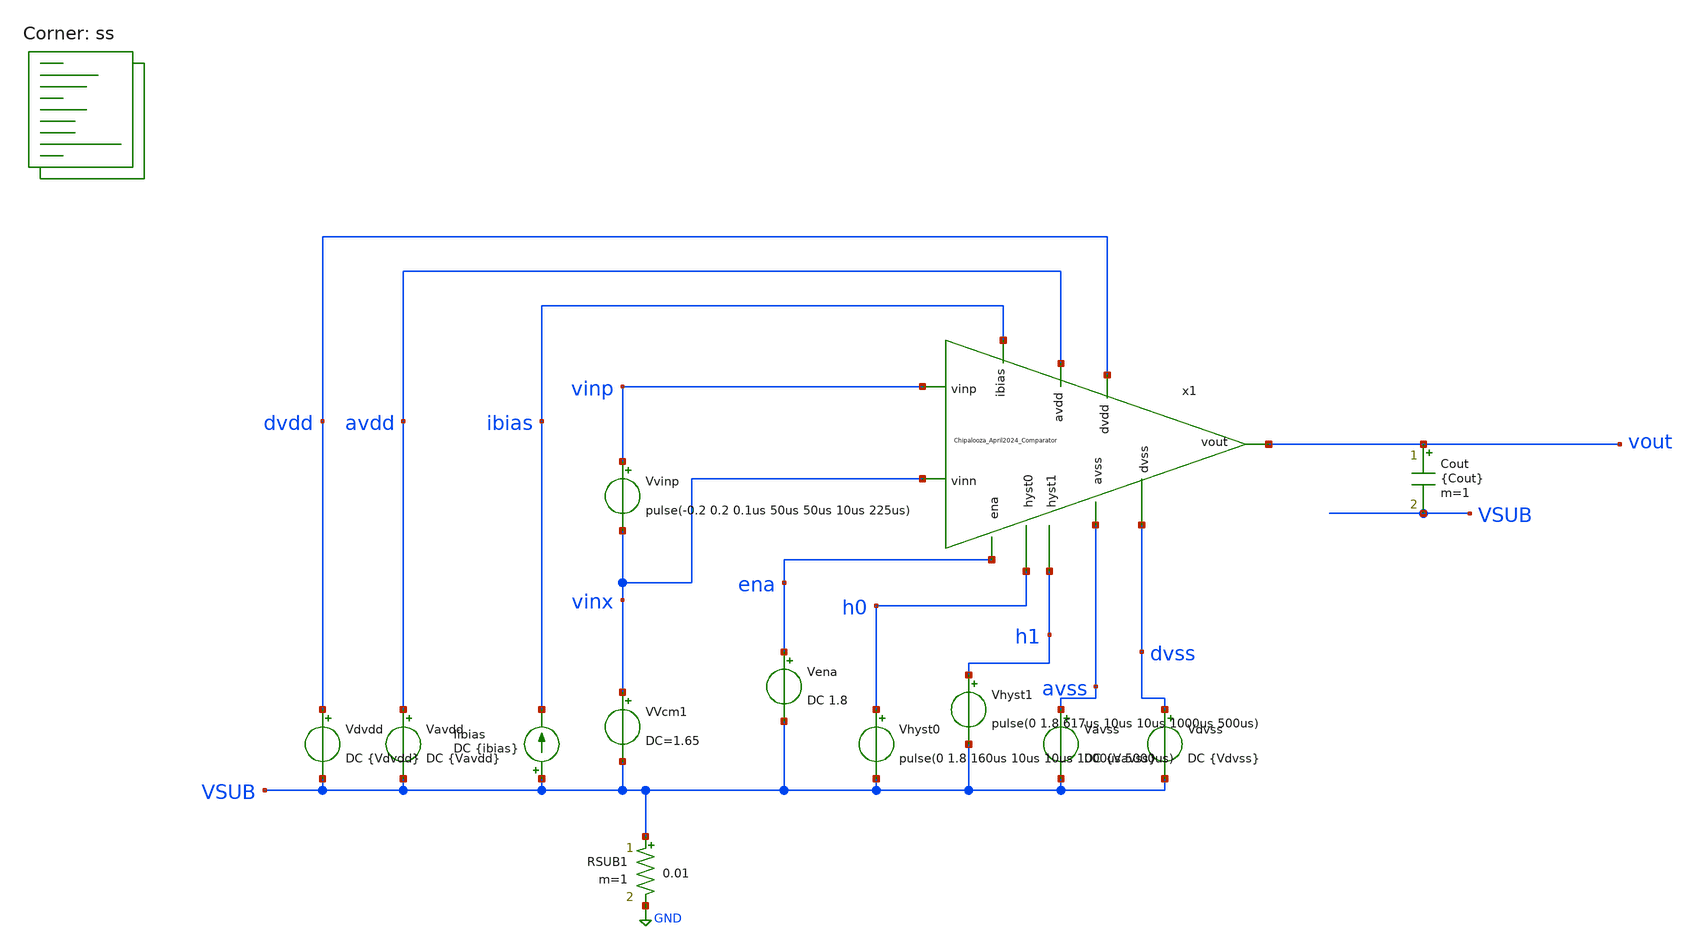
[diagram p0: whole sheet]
** sch_path: Chipalooza_April2024_Comparator/xschem/TB_hysteresis.sch
**.subckt TB_hysteresis
Vavdd avdd VSUB DC {Vavdd}
Vdvdd dvdd VSUB DC {Vdvdd}
Vena ena VSUB DC 1.8
Vhyst0 h0 VSUB pulse(0 1.8 160us 10us 10us 1000us 5000us)
Vhyst1 h1 VSUB pulse(0 1.8 617us 10us 10us 1000us 500us)
Vavss avss VSUB DC {Vavss}
Vdvss dvss VSUB DC {Vdvss}
Iibias VSUB ibias DC {ibias}
RSUB1 VSUB GND 0.01 m=1
VVcm1 vinx VSUB DC=1.65
Vvinp vinp vinx pulse(-0.2 0.2 0.1us 50us 50us 10us 225us)
x1 h0 h1 avdd vinp avss vinx dvdd dvss vout ibias ena Chipalooza_April2024_Comparator
Cout vout VSUB {Cout} m=1
**** begin user architecture code

* this option enables mos model bin
* selection based on W/NF instead of W
*.option wnflag=1
.option savecurrents
.option save all
.option temperature=25

.control

.param vavdd=3.3 cout=0 vdvdd=1.8 vavss=0
.param vdvss=0 ibias=1u

*dc VVcm 0 3.3 0.1
*plot v(vout) v(inx)

tran 0.1u 850u
*plot v(vout) v(vinp)

meas tran tr1 TRIG AT=0u TARG v(vout) VAL=1.75 RISE=1
meas tran vin_tr1 find v(vinp) at=tr1

meas tran tf1 TRIG AT=0u TARG v(vout) VAL=0.05 FALL=1
meas tran vin_tf1 find v(vinp) at=tf1

meas tran tr2 TRIG AT=0u TARG v(vout) VAL=1.75 RISE=2
meas tran vin_tr2 find v(vinp) at=tr1

meas tran tf2 TRIG AT=0u TARG v(vout) VAL=0.05 FALL=2
meas tran vin_tf2 find v(vinp) at=tf2

meas tran tr3 TRIG AT=0u TARG v(vout) VAL=1.75 RISE=3
meas tran vin_tr3 find v(vinp) at=tr3

meas tran tf3 TRIG AT=0u TARG v(vout) VAL=0.05 FALL=3
meas tran vin_tf3 find v(vinp) at=tf3

meas tran tr4 TRIG AT=0u TARG v(vout) VAL=1.75 RISE=4
meas tran vin_tr4 find v(vinp) at=tr4

meas tran tf4 TRIG AT=0u TARG v(vout) VAL=0.05 FALL=4
meas tran vin_tf4 find v(vinp) at=tf4

let hyst1=(vin_tf1-vin_tr1)
let hyst2=(vin_tf2-vin_tr2)
let hyst3=(vin_tf3-vin_tr3)
let hyst4=(vin_tf4-vin_tr4)

print hyst1
print hyst2
print hyst3
print hyst4

meas tran vinx_tr find v(vinx) at=tr1
let vio=(vinx_tr-vin_tr1)

print vio

write TB_hysteresis.raw

echo $&hyst1 $&hyst2 $&hyst3 $&vio > {simpath}/{filename}_{N}.data


*quit 0

.endc


.lib $::SKYWATER_MODELS/sky130.lib.spice ss
**** end user architecture code
**.ends

* expanding   symbol:  Chipalooza_April2024_Comparator.sym # of pins=11
** sym_path: Chipalooza_April2024_Comparator/xschem/Chipalooza_April2024_Comparator.sym
** sch_path: Chipalooza_April2024_Comparator/xschem/Chipalooza_April2024_Comparator.sch
.subckt Chipalooza_April2024_Comparator hyst0 hyst1 avdd vinp avss vinn dvdd dvss vout ibias ena
*.ipin vinp
*.ipin vinn
*.ipin hyst0
*.ipin hyst1
*.ipin avdd
*.ipin avss
*.ipin dvdd
*.ipin dvss
*.opin vout
*.ipin ena
*.ipin ibias
XM29 SumOutBar SumOut dvdd dvdd sky130_fd_pr__pfet_01v8 L=1 W=2 nf=1 ad='int((nf+1)/2) * W/nf * 0.29'
+ as='int((nf+2)/2) * W/nf * 0.29' pd='2*int((nf+1)/2) * (W/nf + 0.29)' ps='2*int((nf+2)/2) * (W/nf + 0.29)'
+ nrd='0.29 / W' nrs='0.29 / W' sa=0 sb=0 sd=0 mult=2 m=2
XM30 SumOutBar SumOut avssi dvss sky130_fd_pr__nfet_01v8 L=1 W=2 nf=1 ad='int((nf+1)/2) * W/nf * 0.29'
+ as='int((nf+2)/2) * W/nf * 0.29' pd='2*int((nf+1)/2) * (W/nf + 0.29)' ps='2*int((nf+2)/2) * (W/nf + 0.29)'
+ nrd='0.29 / W' nrs='0.29 / W' sa=0 sb=0 sd=0 mult=2 m=2
XM25 net3 ibias avssi avss sky130_fd_pr__nfet_g5v0d10v5 L=4 W=1 nf=1 ad='int((nf+1)/2) * W/nf * 0.29'
+ as='int((nf+2)/2) * W/nf * 0.29' pd='2*int((nf+1)/2) * (W/nf + 0.29)' ps='2*int((nf+2)/2) * (W/nf + 0.29)'
+ nrd='0.29 / W' nrs='0.29 / W' sa=0 sb=0 sd=0 mult=2 m=2
C1 avss 0 2p m=1
XM38 avssi ena avss avss sky130_fd_pr__nfet_g5v0d10v5 L=1 W=4 nf=1 ad='int((nf+1)/2) * W/nf * 0.29' as='int((nf+2)/2) * W/nf * 0.29'
+ pd='2*int((nf+1)/2) * (W/nf + 0.29)' ps='2*int((nf+2)/2) * (W/nf + 0.29)' nrd='0.29 / W' nrs='0.29 / W'
+ sa=0 sb=0 sd=0 mult=4 m=4
XM39 net4 ibias avssi avss sky130_fd_pr__nfet_g5v0d10v5 L=1 W=1 nf=1 ad='int((nf+1)/2) * W/nf * 0.29'
+ as='int((nf+2)/2) * W/nf * 0.29' pd='2*int((nf+1)/2) * (W/nf + 0.29)' ps='2*int((nf+2)/2) * (W/nf + 0.29)'
+ nrd='0.29 / W' nrs='0.29 / W' sa=0 sb=0 sd=0 mult=2 m=2
XM16 vout SumOutBar dvdd dvdd sky130_fd_pr__pfet_01v8 L=1 W=2 nf=1 ad='int((nf+1)/2) * W/nf * 0.29' as='int((nf+2)/2) * W/nf * 0.29'
+ pd='2*int((nf+1)/2) * (W/nf + 0.29)' ps='2*int((nf+2)/2) * (W/nf + 0.29)' nrd='0.29 / W' nrs='0.29 / W'
+ sa=0 sb=0 sd=0 mult=2 m=2
XM18 vout SumOutBar avssi dvss sky130_fd_pr__nfet_01v8 L=1 W=2 nf=1 ad='int((nf+1)/2) * W/nf * 0.29'
+ as='int((nf+2)/2) * W/nf * 0.29' pd='2*int((nf+1)/2) * (W/nf + 0.29)' ps='2*int((nf+2)/2) * (W/nf + 0.29)'
+ nrd='0.29 / W' nrs='0.29 / W' sa=0 sb=0 sd=0 mult=2 m=2
XM4 SourceBias2 SourceBias2 avdd avdd sky130_fd_pr__pfet_g5v0d10v5 L=1 W=2 nf=1 ad='int((nf+1)/2) * W/nf * 0.29'
+ as='int((nf+2)/2) * W/nf * 0.29' pd='2*int((nf+1)/2) * (W/nf + 0.29)' ps='2*int((nf+2)/2) * (W/nf + 0.29)'
+ nrd='0.29 / W' nrs='0.29 / W' sa=0 sb=0 sd=0 mult=2 m=2
XM5 N1 SourceBias2 avdd avdd sky130_fd_pr__pfet_g5v0d10v5 L=1 W=2 nf=1 ad='int((nf+1)/2) * W/nf * 0.29'
+ as='int((nf+2)/2) * W/nf * 0.29' pd='2*int((nf+1)/2) * (W/nf + 0.29)' ps='2*int((nf+2)/2) * (W/nf + 0.29)'
+ nrd='0.29 / W' nrs='0.29 / W' sa=0 sb=0 sd=0 mult=2 m=2
XM6 N2 SourceBias2 avdd avdd sky130_fd_pr__pfet_g5v0d10v5 L=1 W=2 nf=1 ad='int((nf+1)/2) * W/nf * 0.29'
+ as='int((nf+2)/2) * W/nf * 0.29' pd='2*int((nf+1)/2) * (W/nf + 0.29)' ps='2*int((nf+2)/2) * (W/nf + 0.29)'
+ nrd='0.29 / W' nrs='0.29 / W' sa=0 sb=0 sd=0 mult=2 m=2
XM7 SumOut Bias1 N2 avdd sky130_fd_pr__pfet_g5v0d10v5 L=1 W=2 nf=1 ad='int((nf+1)/2) * W/nf * 0.29' as='int((nf+2)/2) * W/nf * 0.29'
+ pd='2*int((nf+1)/2) * (W/nf + 0.29)' ps='2*int((nf+2)/2) * (W/nf + 0.29)' nrd='0.29 / W' nrs='0.29 / W'
+ sa=0 sb=0 sd=0 mult=2 m=2
XM8 Sum Bias1 N1 avdd sky130_fd_pr__pfet_g5v0d10v5 L=1 W=2 nf=1 ad='int((nf+1)/2) * W/nf * 0.29' as='int((nf+2)/2) * W/nf * 0.29'
+ pd='2*int((nf+1)/2) * (W/nf + 0.29)' ps='2*int((nf+2)/2) * (W/nf + 0.29)' nrd='0.29 / W' nrs='0.29 / W'
+ sa=0 sb=0 sd=0 mult=2 m=2
XM9 SumOut Bias2 P2 avss sky130_fd_pr__nfet_g5v0d10v5 L=1 W=2 nf=1 ad='int((nf+1)/2) * W/nf * 0.29' as='int((nf+2)/2) * W/nf * 0.29'
+ pd='2*int((nf+1)/2) * (W/nf + 0.29)' ps='2*int((nf+2)/2) * (W/nf + 0.29)' nrd='0.29 / W' nrs='0.29 / W'
+ sa=0 sb=0 sd=0 mult=2 m=2
XM10 Sum Bias2 P1 avss sky130_fd_pr__nfet_g5v0d10v5 L=1 W=2 nf=1 ad='int((nf+1)/2) * W/nf * 0.29' as='int((nf+2)/2) * W/nf * 0.29'
+ pd='2*int((nf+1)/2) * (W/nf + 0.29)' ps='2*int((nf+2)/2) * (W/nf + 0.29)' nrd='0.29 / W' nrs='0.29 / W'
+ sa=0 sb=0 sd=0 mult=2 m=2
XM11 P2 Sum avssi avss sky130_fd_pr__nfet_g5v0d10v5 L=1 W=2 nf=1 ad='int((nf+1)/2) * W/nf * 0.29' as='int((nf+2)/2) * W/nf * 0.29'
+ pd='2*int((nf+1)/2) * (W/nf + 0.29)' ps='2*int((nf+2)/2) * (W/nf + 0.29)' nrd='0.29 / W' nrs='0.29 / W'
+ sa=0 sb=0 sd=0 mult=2 m=2
XM12 P1 Sum avssi avss sky130_fd_pr__nfet_g5v0d10v5 L=1 W=2 nf=1 ad='int((nf+1)/2) * W/nf * 0.29' as='int((nf+2)/2) * W/nf * 0.29'
+ pd='2*int((nf+1)/2) * (W/nf + 0.29)' ps='2*int((nf+2)/2) * (W/nf + 0.29)' nrd='0.29 / W' nrs='0.29 / W'
+ sa=0 sb=0 sd=0 mult=2 m=2
XM2 P2 vinn psource_input avdd sky130_fd_pr__pfet_g5v0d10v5 L=1 W=4 nf=1 ad='int((nf+1)/2) * W/nf * 0.29'
+ as='int((nf+2)/2) * W/nf * 0.29' pd='2*int((nf+1)/2) * (W/nf + 0.29)' ps='2*int((nf+2)/2) * (W/nf + 0.29)'
+ nrd='0.29 / W' nrs='0.29 / W' sa=0 sb=0 sd=0 mult=2 m=2
XM3 P1 vinp psource_input avdd sky130_fd_pr__pfet_g5v0d10v5 L=1 W=4 nf=1 ad='int((nf+1)/2) * W/nf * 0.29'
+ as='int((nf+2)/2) * W/nf * 0.29' pd='2*int((nf+1)/2) * (W/nf + 0.29)' ps='2*int((nf+2)/2) * (W/nf + 0.29)'
+ nrd='0.29 / W' nrs='0.29 / W' sa=0 sb=0 sd=0 mult=2 m=2
XM14 psource_input net5 avdd avdd sky130_fd_pr__pfet_g5v0d10v5 L=1 W=12 nf=1 ad='int((nf+1)/2) * W/nf * 0.29'
+ as='int((nf+2)/2) * W/nf * 0.29' pd='2*int((nf+1)/2) * (W/nf + 0.29)' ps='2*int((nf+2)/2) * (W/nf + 0.29)'
+ nrd='0.29 / W' nrs='0.29 / W' sa=0 sb=0 sd=0 mult=4 m=4
XM15 net5 net5 avdd avdd sky130_fd_pr__pfet_g5v0d10v5 L=1 W=8 nf=1 ad='int((nf+1)/2) * W/nf * 0.29' as='int((nf+2)/2) * W/nf * 0.29'
+ pd='2*int((nf+1)/2) * (W/nf + 0.29)' ps='2*int((nf+2)/2) * (W/nf + 0.29)' nrd='0.29 / W' nrs='0.29 / W'
+ sa=0 sb=0 sd=0 mult=2 m=2
XM17 nbias_tail net10 psource_input avdd sky130_fd_pr__pfet_g5v0d10v5 L=1 W=8 nf=1 ad='int((nf+1)/2) * W/nf * 0.29'
+ as='int((nf+2)/2) * W/nf * 0.29' pd='2*int((nf+1)/2) * (W/nf + 0.29)' ps='2*int((nf+2)/2) * (W/nf + 0.29)'
+ nrd='0.29 / W' nrs='0.29 / W' sa=0 sb=0 sd=0 mult=2 m=2
XM20 N1 vinp SourceBias0 avss sky130_fd_pr__nfet_g5v0d10v5 L=4 W=16 nf=1 ad='int((nf+1)/2) * W/nf * 0.29'
+ as='int((nf+2)/2) * W/nf * 0.29' pd='2*int((nf+1)/2) * (W/nf + 0.29)' ps='2*int((nf+2)/2) * (W/nf + 0.29)'
+ nrd='0.29 / W' nrs='0.29 / W' sa=0 sb=0 sd=0 mult=2 m=2
XM21 N2 vinn SourceBias0 avss sky130_fd_pr__nfet_g5v0d10v5 L=4 W=16 nf=1 ad='int((nf+1)/2) * W/nf * 0.29'
+ as='int((nf+2)/2) * W/nf * 0.29' pd='2*int((nf+1)/2) * (W/nf + 0.29)' ps='2*int((nf+2)/2) * (W/nf + 0.29)'
+ nrd='0.29 / W' nrs='0.29 / W' sa=0 sb=0 sd=0 mult=2 m=2
XM22 SourceBias0 nbias_tail avssi avss sky130_fd_pr__nfet_g5v0d10v5 L=1 W=12 nf=1 ad='int((nf+1)/2) * W/nf * 0.29'
+ as='int((nf+2)/2) * W/nf * 0.29' pd='2*int((nf+1)/2) * (W/nf + 0.29)' ps='2*int((nf+2)/2) * (W/nf + 0.29)'
+ nrd='0.29 / W' nrs='0.29 / W' sa=0 sb=0 sd=0 mult=4 m=4
XM23 nbias_tail nbias_tail avssi avss sky130_fd_pr__nfet_g5v0d10v5 L=1 W=12 nf=1 ad='int((nf+1)/2) * W/nf * 0.29'
+ as='int((nf+2)/2) * W/nf * 0.29' pd='2*int((nf+1)/2) * (W/nf + 0.29)' ps='2*int((nf+2)/2) * (W/nf + 0.29)'
+ nrd='0.29 / W' nrs='0.29 / W' sa=0 sb=0 sd=0 mult=2 m=2
XM28 net5 Bias5 SourceBias0 avss sky130_fd_pr__nfet_g5v0d10v5 L=1 W=4 nf=1 ad='int((nf+1)/2) * W/nf * 0.29'
+ as='int((nf+2)/2) * W/nf * 0.29' pd='2*int((nf+1)/2) * (W/nf + 0.29)' ps='2*int((nf+2)/2) * (W/nf + 0.29)'
+ nrd='0.29 / W' nrs='0.29 / W' sa=0 sb=0 sd=0 mult=2 m=2
XM45 SourceBias1 ibias avssi avss sky130_fd_pr__nfet_g5v0d10v5 L=1 W=3 nf=1 ad='int((nf+1)/2) * W/nf * 0.29'
+ as='int((nf+2)/2) * W/nf * 0.29' pd='2*int((nf+1)/2) * (W/nf + 0.29)' ps='2*int((nf+2)/2) * (W/nf + 0.29)'
+ nrd='0.29 / W' nrs='0.29 / W' sa=0 sb=0 sd=0 mult=2 m=2
XM46 SourceBias1 SourceBias1 avdd avdd sky130_fd_pr__pfet_g5v0d10v5 L=1 W=12 nf=1 ad='int((nf+1)/2) * W/nf * 0.29'
+ as='int((nf+2)/2) * W/nf * 0.29' pd='2*int((nf+1)/2) * (W/nf + 0.29)' ps='2*int((nf+2)/2) * (W/nf + 0.29)'
+ nrd='0.29 / W' nrs='0.29 / W' sa=0 sb=0 sd=0 mult=4 m=4
XM47 psource_input SourceBias1 avdd avdd sky130_fd_pr__pfet_g5v0d10v5 L=1 W=12 nf=1 ad='int((nf+1)/2) * W/nf * 0.29'
+ as='int((nf+2)/2) * W/nf * 0.29' pd='2*int((nf+1)/2) * (W/nf + 0.29)' ps='2*int((nf+2)/2) * (W/nf + 0.29)'
+ nrd='0.29 / W' nrs='0.29 / W' sa=0 sb=0 sd=0 mult=4 m=4
XM48 SourceBias2 ibias avssi avss sky130_fd_pr__nfet_g5v0d10v5 L=1 W=6 nf=1 ad='int((nf+1)/2) * W/nf * 0.29'
+ as='int((nf+2)/2) * W/nf * 0.29' pd='2*int((nf+1)/2) * (W/nf + 0.29)' ps='2*int((nf+2)/2) * (W/nf + 0.29)'
+ nrd='0.29 / W' nrs='0.29 / W' sa=0 sb=0 sd=0 mult=2 m=2
XM65 SourceBias3 ibias avssi avss sky130_fd_pr__nfet_g5v0d10v5 L=1 W=1 nf=1 ad='int((nf+1)/2) * W/nf * 0.29'
+ as='int((nf+2)/2) * W/nf * 0.29' pd='2*int((nf+1)/2) * (W/nf + 0.29)' ps='2*int((nf+2)/2) * (W/nf + 0.29)'
+ nrd='0.29 / W' nrs='0.29 / W' sa=0 sb=0 sd=0 mult=2 m=2
XM76 Bias1 ibias avssi avss sky130_fd_pr__nfet_g5v0d10v5 L=1 W=3 nf=1 ad='int((nf+1)/2) * W/nf * 0.29'
+ as='int((nf+2)/2) * W/nf * 0.29' pd='2*int((nf+1)/2) * (W/nf + 0.29)' ps='2*int((nf+2)/2) * (W/nf + 0.29)'
+ nrd='0.29 / W' nrs='0.29 / W' sa=0 sb=0 sd=0 mult=2 m=2
XM77 SourceBias5 ibias avssi avss sky130_fd_pr__nfet_g5v0d10v5 L=1 W=3 nf=1 ad='int((nf+1)/2) * W/nf * 0.29'
+ as='int((nf+2)/2) * W/nf * 0.29' pd='2*int((nf+1)/2) * (W/nf + 0.29)' ps='2*int((nf+2)/2) * (W/nf + 0.29)'
+ nrd='0.29 / W' nrs='0.29 / W' sa=0 sb=0 sd=0 mult=2 m=2
XM78 SourceBias6 ibias avssi avss sky130_fd_pr__nfet_g5v0d10v5 L=1 W=3 nf=1 ad='int((nf+1)/2) * W/nf * 0.29'
+ as='int((nf+2)/2) * W/nf * 0.29' pd='2*int((nf+1)/2) * (W/nf + 0.29)' ps='2*int((nf+2)/2) * (W/nf + 0.29)'
+ nrd='0.29 / W' nrs='0.29 / W' sa=0 sb=0 sd=0 mult=2 m=2
XM79 SourceBias7 ibias avssi avss sky130_fd_pr__nfet_g5v0d10v5 L=1 W=3 nf=1 ad='int((nf+1)/2) * W/nf * 0.29'
+ as='int((nf+2)/2) * W/nf * 0.29' pd='2*int((nf+1)/2) * (W/nf + 0.29)' ps='2*int((nf+2)/2) * (W/nf + 0.29)'
+ nrd='0.29 / W' nrs='0.29 / W' sa=0 sb=0 sd=0 mult=2 m=2
XM81 Bias5 ibias avssi avss sky130_fd_pr__nfet_g5v0d10v5 L=1 W=3 nf=1 ad='int((nf+1)/2) * W/nf * 0.29'
+ as='int((nf+2)/2) * W/nf * 0.29' pd='2*int((nf+1)/2) * (W/nf + 0.29)' ps='2*int((nf+2)/2) * (W/nf + 0.29)'
+ nrd='0.29 / W' nrs='0.29 / W' sa=0 sb=0 sd=0 mult=2 m=2
XM54 M55Source M55Drain avssi avss sky130_fd_pr__nfet_g5v0d10v5 L=1.5 W=6 nf=1 ad='int((nf+1)/2) * W/nf * 0.29'
+ as='int((nf+2)/2) * W/nf * 0.29' pd='2*int((nf+1)/2) * (W/nf + 0.29)' ps='2*int((nf+2)/2) * (W/nf + 0.29)'
+ nrd='0.29 / W' nrs='0.29 / W' sa=0 sb=0 sd=0 mult=2 m=2
XM55 M55Drain Bias2 M55Source avss sky130_fd_pr__nfet_g5v0d10v5 L=1 W=9 nf=1 ad='int((nf+1)/2) * W/nf * 0.29'
+ as='int((nf+2)/2) * W/nf * 0.29' pd='2*int((nf+1)/2) * (W/nf + 0.29)' ps='2*int((nf+2)/2) * (W/nf + 0.29)'
+ nrd='0.29 / W' nrs='0.29 / W' sa=0 sb=0 sd=0 mult=2 m=2
XM56 Bias2 Bias2 avssi avss sky130_fd_pr__nfet_g5v0d10v5 L=2 W=0.5 nf=1 ad='int((nf+1)/2) * W/nf * 0.29'
+ as='int((nf+2)/2) * W/nf * 0.29' pd='2*int((nf+1)/2) * (W/nf + 0.29)' ps='2*int((nf+2)/2) * (W/nf + 0.29)'
+ nrd='0.29 / W' nrs='0.29 / W' sa=0 sb=0 sd=0 mult=1 m=1
XM51 net6 net7 avdd avdd sky130_fd_pr__pfet_g5v0d10v5 L=2 W=20 nf=1 ad='int((nf+1)/2) * W/nf * 0.29'
+ as='int((nf+2)/2) * W/nf * 0.29' pd='2*int((nf+1)/2) * (W/nf + 0.29)' ps='2*int((nf+2)/2) * (W/nf + 0.29)'
+ nrd='0.29 / W' nrs='0.29 / W' sa=0 sb=0 sd=0 mult=2 m=2
XM49 net7 net7 avdd avdd sky130_fd_pr__pfet_g5v0d10v5 L=2 W=10 nf=1 ad='int((nf+1)/2) * W/nf * 0.29'
+ as='int((nf+2)/2) * W/nf * 0.29' pd='2*int((nf+1)/2) * (W/nf + 0.29)' ps='2*int((nf+2)/2) * (W/nf + 0.29)'
+ nrd='0.29 / W' nrs='0.29 / W' sa=0 sb=0 sd=0 mult=2 m=2
XM50 SourceBias4 SourceBias4 net7 avdd sky130_fd_pr__pfet_g5v0d10v5 L=1 W=10 nf=1 ad='int((nf+1)/2) * W/nf * 0.29'
+ as='int((nf+2)/2) * W/nf * 0.29' pd='2*int((nf+1)/2) * (W/nf + 0.29)' ps='2*int((nf+2)/2) * (W/nf + 0.29)'
+ nrd='0.29 / W' nrs='0.29 / W' sa=0 sb=0 sd=0 mult=2 m=2
XM52 avssi SourceBias4 net6 avdd sky130_fd_pr__pfet_g5v0d10v5 L=1 W=1 nf=1 ad='int((nf+1)/2) * W/nf * 0.29'
+ as='int((nf+2)/2) * W/nf * 0.29' pd='2*int((nf+1)/2) * (W/nf + 0.29)' ps='2*int((nf+2)/2) * (W/nf + 0.29)'
+ nrd='0.29 / W' nrs='0.29 / W' sa=0 sb=0 sd=0 mult=2 m=2
XM53 Bias1 Bias1 net6 avdd sky130_fd_pr__pfet_g5v0d10v5 L=1 W=5 nf=1 ad='int((nf+1)/2) * W/nf * 0.29'
+ as='int((nf+2)/2) * W/nf * 0.29' pd='2*int((nf+1)/2) * (W/nf + 0.29)' ps='2*int((nf+2)/2) * (W/nf + 0.29)'
+ nrd='0.29 / W' nrs='0.29 / W' sa=0 sb=0 sd=0 mult=2 m=2
XM66 net8 net9 avdd avdd sky130_fd_pr__pfet_g5v0d10v5 L=2 W=20 nf=1 ad='int((nf+1)/2) * W/nf * 0.29'
+ as='int((nf+2)/2) * W/nf * 0.29' pd='2*int((nf+1)/2) * (W/nf + 0.29)' ps='2*int((nf+2)/2) * (W/nf + 0.29)'
+ nrd='0.29 / W' nrs='0.29 / W' sa=0 sb=0 sd=0 mult=2 m=2
XM67 net9 net9 avdd avdd sky130_fd_pr__pfet_g5v0d10v5 L=2 W=20 nf=1 ad='int((nf+1)/2) * W/nf * 0.29'
+ as='int((nf+2)/2) * W/nf * 0.29' pd='2*int((nf+1)/2) * (W/nf + 0.29)' ps='2*int((nf+2)/2) * (W/nf + 0.29)'
+ nrd='0.29 / W' nrs='0.29 / W' sa=0 sb=0 sd=0 mult=2 m=2
XM68 SourceBias7 SourceBias7 net9 avdd sky130_fd_pr__pfet_g5v0d10v5 L=1 W=10 nf=1 ad='int((nf+1)/2) * W/nf * 0.29'
+ as='int((nf+2)/2) * W/nf * 0.29' pd='2*int((nf+1)/2) * (W/nf + 0.29)' ps='2*int((nf+2)/2) * (W/nf + 0.29)'
+ nrd='0.29 / W' nrs='0.29 / W' sa=0 sb=0 sd=0 mult=2 m=2
XM69 avssi SourceBias7 net8 avdd sky130_fd_pr__pfet_g5v0d10v5 L=1 W=1 nf=1 ad='int((nf+1)/2) * W/nf * 0.29'
+ as='int((nf+2)/2) * W/nf * 0.29' pd='2*int((nf+1)/2) * (W/nf + 0.29)' ps='2*int((nf+2)/2) * (W/nf + 0.29)'
+ nrd='0.29 / W' nrs='0.29 / W' sa=0 sb=0 sd=0 mult=2 m=2
XM70 Bias5 Bias5 net8 avdd sky130_fd_pr__pfet_g5v0d10v5 L=1 W=5 nf=1 ad='int((nf+1)/2) * W/nf * 0.29'
+ as='int((nf+2)/2) * W/nf * 0.29' pd='2*int((nf+1)/2) * (W/nf + 0.29)' ps='2*int((nf+2)/2) * (W/nf + 0.29)'
+ nrd='0.29 / W' nrs='0.29 / W' sa=0 sb=0 sd=0 mult=2 m=2
XM72 SourceBias5 SourceBias5 avdd avdd sky130_fd_pr__pfet_g5v0d10v5 L=1 W=12 nf=1 ad='int((nf+1)/2) * W/nf * 0.29'
+ as='int((nf+2)/2) * W/nf * 0.29' pd='2*int((nf+1)/2) * (W/nf + 0.29)' ps='2*int((nf+2)/2) * (W/nf + 0.29)'
+ nrd='0.29 / W' nrs='0.29 / W' sa=0 sb=0 sd=0 mult=4 m=4
XM73 M55Drain SourceBias5 avdd avdd sky130_fd_pr__pfet_g5v0d10v5 L=1 W=12 nf=1 ad='int((nf+1)/2) * W/nf * 0.29'
+ as='int((nf+2)/2) * W/nf * 0.29' pd='2*int((nf+1)/2) * (W/nf + 0.29)' ps='2*int((nf+2)/2) * (W/nf + 0.29)'
+ nrd='0.29 / W' nrs='0.29 / W' sa=0 sb=0 sd=0 mult=4 m=4
XM74 SourceBias6 SourceBias6 avdd avdd sky130_fd_pr__pfet_g5v0d10v5 L=1 W=12 nf=1 ad='int((nf+1)/2) * W/nf * 0.29'
+ as='int((nf+2)/2) * W/nf * 0.29' pd='2*int((nf+1)/2) * (W/nf + 0.29)' ps='2*int((nf+2)/2) * (W/nf + 0.29)'
+ nrd='0.29 / W' nrs='0.29 / W' sa=0 sb=0 sd=0 mult=4 m=4
XM75 Bias2 SourceBias6 avdd avdd sky130_fd_pr__pfet_g5v0d10v5 L=1 W=12 nf=1 ad='int((nf+1)/2) * W/nf * 0.29'
+ as='int((nf+2)/2) * W/nf * 0.29' pd='2*int((nf+1)/2) * (W/nf + 0.29)' ps='2*int((nf+2)/2) * (W/nf + 0.29)'
+ nrd='0.29 / W' nrs='0.29 / W' sa=0 sb=0 sd=0 mult=4 m=4
XM1 SourceBias0 ibias avssi avss sky130_fd_pr__nfet_g5v0d10v5 L=1 W=3 nf=1 ad='int((nf+1)/2) * W/nf * 0.29'
+ as='int((nf+2)/2) * W/nf * 0.29' pd='2*int((nf+1)/2) * (W/nf + 0.29)' ps='2*int((nf+2)/2) * (W/nf + 0.29)'
+ nrd='0.29 / W' nrs='0.29 / W' sa=0 sb=0 sd=0 mult=2 m=2
XM31 net1 hyst0 net3 avss sky130_fd_pr__nfet_01v8 L=4 W=1 nf=1 ad='int((1 + 1)/2) * 1 / 1 * 0.29' as='int((1 + 2)/2) * 1 / 1 * 0.29'
+ pd='2*int((1 + 1)/2) * (1 / 1 + 0.29)' ps='2*int((1 + 2)/2) * (1 / 1 + 0.29)' nrd='0.29 / 1 ' nrs='0.29 / 1 '
+ sa=0 sb=0 sd=0 mult=2 m=2
XM32 net1 hyst1 net4 avss sky130_fd_pr__nfet_01v8 L=1 W=1 nf=1 ad='int((1 + 1)/2) * 1 / 1 * 0.29' as='int((1 + 2)/2) * 1 / 1 * 0.29'
+ pd='2*int((1 + 1)/2) * (1 / 1 + 0.29)' ps='2*int((1 + 2)/2) * (1 / 1 + 0.29)' nrd='0.29 / 1 ' nrs='0.29 / 1 '
+ sa=0 sb=0 sd=0 mult=2 m=2
XM19 N1 SumOut net1 avss sky130_fd_pr__nfet_g5v0d10v5 L=1 W=2 nf=1 ad='int((nf+1)/2) * W/nf * 0.29' as='int((nf+2)/2) * W/nf * 0.29'
+ pd='2*int((nf+1)/2) * (W/nf + 0.29)' ps='2*int((nf+2)/2) * (W/nf + 0.29)' nrd='0.29 / W' nrs='0.29 / W'
+ sa=0 sb=0 sd=0 mult=2 m=2
XM24 N2 SumOutBar net1 avss sky130_fd_pr__nfet_g5v0d10v5 L=1 W=2 nf=1 ad='int((nf+1)/2) * W/nf * 0.29'
+ as='int((nf+2)/2) * W/nf * 0.29' pd='2*int((nf+1)/2) * (W/nf + 0.29)' ps='2*int((nf+2)/2) * (W/nf + 0.29)'
+ nrd='0.29 / W' nrs='0.29 / W' sa=0 sb=0 sd=0 mult=2 m=2
XM26 ibias ibias avssi avss sky130_fd_pr__nfet_g5v0d10v5 L=1 W=3 nf=1 ad='int((nf+1)/2) * W/nf * 0.29'
+ as='int((nf+2)/2) * W/nf * 0.29' pd='2*int((nf+1)/2) * (W/nf + 0.29)' ps='2*int((nf+2)/2) * (W/nf + 0.29)'
+ nrd='0.29 / W' nrs='0.29 / W' sa=0 sb=0 sd=0 mult=2 m=2
XM27 net2 ibias avssi avss sky130_fd_pr__nfet_g5v0d10v5 L=1 W=3 nf=1 ad='int((nf+1)/2) * W/nf * 0.29'
+ as='int((nf+2)/2) * W/nf * 0.29' pd='2*int((nf+1)/2) * (W/nf + 0.29)' ps='2*int((nf+2)/2) * (W/nf + 0.29)'
+ nrd='0.29 / W' nrs='0.29 / W' sa=0 sb=0 sd=0 mult=2 m=2
XM33 net2 net2 avdd avdd sky130_fd_pr__pfet_g5v0d10v5 L=1 W=3 nf=1 ad='int((nf+1)/2) * W/nf * 0.29' as='int((nf+2)/2) * W/nf * 0.29'
+ pd='2*int((nf+1)/2) * (W/nf + 0.29)' ps='2*int((nf+2)/2) * (W/nf + 0.29)' nrd='0.29 / W' nrs='0.29 / W'
+ sa=0 sb=0 sd=0 mult=2 m=2
XM34 avss net2 avdd avdd sky130_fd_pr__pfet_g5v0d10v5 L=1 W=3 nf=1 ad='int((nf+1)/2) * W/nf * 0.29' as='int((nf+2)/2) * W/nf * 0.29'
+ pd='2*int((nf+1)/2) * (W/nf + 0.29)' ps='2*int((nf+2)/2) * (W/nf + 0.29)' nrd='0.29 / W' nrs='0.29 / W'
+ sa=0 sb=0 sd=0 mult=2 m=2
XM63 net10 net10 avdd avdd sky130_fd_pr__pfet_g5v0d10v5 L=5 W=3 nf=1 ad='int((nf+1)/2) * W/nf * 0.29'
+ as='int((nf+2)/2) * W/nf * 0.29' pd='2*int((nf+1)/2) * (W/nf + 0.29)' ps='2*int((nf+2)/2) * (W/nf + 0.29)'
+ nrd='0.29 / W' nrs='0.29 / W' sa=0 sb=0 sd=0 mult=1 m=1
XM62 avdd Bias4 SourceBias3 avss sky130_fd_pr__nfet_g5v0d10v5 L=1 W=4 nf=1 ad='int((nf+1)/2) * W/nf * 0.29'
+ as='int((nf+2)/2) * W/nf * 0.29' pd='2*int((nf+1)/2) * (W/nf + 0.29)' ps='2*int((nf+2)/2) * (W/nf + 0.29)'
+ nrd='0.29 / W' nrs='0.29 / W' sa=0 sb=0 sd=0 mult=2 m=2
XM64 net10 Bias5 SourceBias3 avss sky130_fd_pr__nfet_g5v0d10v5 L=1 W=4 nf=1 ad='int((nf+1)/2) * W/nf * 0.29'
+ as='int((nf+2)/2) * W/nf * 0.29' pd='2*int((nf+1)/2) * (W/nf + 0.29)' ps='2*int((nf+2)/2) * (W/nf + 0.29)'
+ nrd='0.29 / W' nrs='0.29 / W' sa=0 sb=0 sd=0 mult=2 m=2
XM57 net11 net12 avdd avdd sky130_fd_pr__pfet_g5v0d10v5 L=2 W=20 nf=1 ad='int((nf+1)/2) * W/nf * 0.29'
+ as='int((nf+2)/2) * W/nf * 0.29' pd='2*int((nf+1)/2) * (W/nf + 0.29)' ps='2*int((nf+2)/2) * (W/nf + 0.29)'
+ nrd='0.29 / W' nrs='0.29 / W' sa=0 sb=0 sd=0 mult=2 m=2
XM58 net12 net12 avdd avdd sky130_fd_pr__pfet_g5v0d10v5 L=2 W=10 nf=1 ad='int((nf+1)/2) * W/nf * 0.29'
+ as='int((nf+2)/2) * W/nf * 0.29' pd='2*int((nf+1)/2) * (W/nf + 0.29)' ps='2*int((nf+2)/2) * (W/nf + 0.29)'
+ nrd='0.29 / W' nrs='0.29 / W' sa=0 sb=0 sd=0 mult=2 m=2
XM59 SourceBias10 SourceBias10 net12 avdd sky130_fd_pr__pfet_g5v0d10v5 L=1 W=10 nf=1 ad='int((nf+1)/2) * W/nf * 0.29'
+ as='int((nf+2)/2) * W/nf * 0.29' pd='2*int((nf+1)/2) * (W/nf + 0.29)' ps='2*int((nf+2)/2) * (W/nf + 0.29)'
+ nrd='0.29 / W' nrs='0.29 / W' sa=0 sb=0 sd=0 mult=2 m=2
XM60 avss SourceBias10 net11 avdd sky130_fd_pr__pfet_g5v0d10v5 L=1 W=1 nf=1 ad='int((nf+1)/2) * W/nf * 0.29'
+ as='int((nf+2)/2) * W/nf * 0.29' pd='2*int((nf+1)/2) * (W/nf + 0.29)' ps='2*int((nf+2)/2) * (W/nf + 0.29)'
+ nrd='0.29 / W' nrs='0.29 / W' sa=0 sb=0 sd=0 mult=2 m=2
XM61 Bias4 Bias4 net11 avdd sky130_fd_pr__pfet_g5v0d10v5 L=1 W=5 nf=1 ad='int((nf+1)/2) * W/nf * 0.29'
+ as='int((nf+2)/2) * W/nf * 0.29' pd='2*int((nf+1)/2) * (W/nf + 0.29)' ps='2*int((nf+2)/2) * (W/nf + 0.29)'
+ nrd='0.29 / W' nrs='0.29 / W' sa=0 sb=0 sd=0 mult=2 m=2
XM13 Bias4 ibias avssi avss sky130_fd_pr__nfet_g5v0d10v5 L=1 W=3 nf=1 ad='int((nf+1)/2) * W/nf * 0.29'
+ as='int((nf+2)/2) * W/nf * 0.29' pd='2*int((nf+1)/2) * (W/nf + 0.29)' ps='2*int((nf+2)/2) * (W/nf + 0.29)'
+ nrd='0.29 / W' nrs='0.29 / W' sa=0 sb=0 sd=0 mult=2 m=2
XM35 SourceBias10 ibias avssi avss sky130_fd_pr__nfet_g5v0d10v5 L=1 W=3 nf=1 ad='int((nf+1)/2) * W/nf * 0.29'
+ as='int((nf+2)/2) * W/nf * 0.29' pd='2*int((nf+1)/2) * (W/nf + 0.29)' ps='2*int((nf+2)/2) * (W/nf + 0.29)'
+ nrd='0.29 / W' nrs='0.29 / W' sa=0 sb=0 sd=0 mult=2 m=2
XM36 SourceBias4 ibias avssi avss sky130_fd_pr__nfet_g5v0d10v5 L=1 W=3 nf=1 ad='int((nf+1)/2) * W/nf * 0.29'
+ as='int((nf+2)/2) * W/nf * 0.29' pd='2*int((nf+1)/2) * (W/nf + 0.29)' ps='2*int((nf+2)/2) * (W/nf + 0.29)'
+ nrd='0.29 / W' nrs='0.29 / W' sa=0 sb=0 sd=0 mult=2 m=2
.ends

.GLOBAL GND
.end
